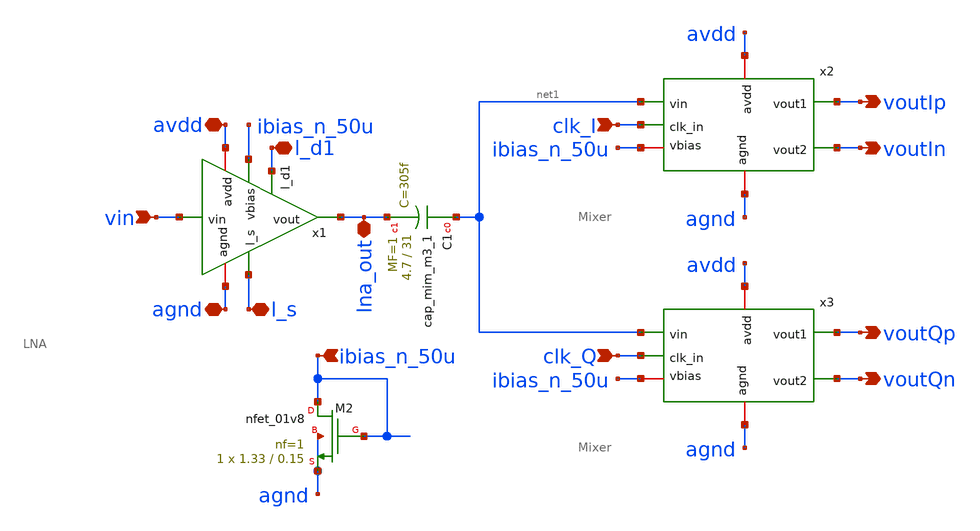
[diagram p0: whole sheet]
** sch_path: Testbenches/LNA_Mixer.sch
**.subckt LNA_Mixer lna_out avdd l_s clk_I clk_Q voutIp voutIn voutQp voutQn vin l_d1 agnd
*+ ibias_n_50u
*.iopin lna_out
*.iopin avdd
*.iopin l_s
*.ipin clk_I
*.ipin clk_Q
*.opin voutIp
*.opin voutIn
*.opin voutQp
*.opin voutQn
*.ipin vin
*.iopin l_d1
*.iopin agnd
*.ipin ibias_n_50u
XC1 net1 lna_out sky130_fd_pr__cap_mim_m3_1 W=4.7 L=31 MF=1 m=1
XM2 ibias_n_50u ibias_n_50u agnd agnd sky130_fd_pr__nfet_01v8 L=0.15 W=1.33 nf=1 ad='int((nf+1)/2) * W/nf * 0.29'
+ as='int((nf+2)/2) * W/nf * 0.29' pd='2*int((nf+1)/2) * (W/nf + 0.29)' ps='2*int((nf+2)/2) * (W/nf + 0.29)'
+ nrd='0.29 / W' nrs='0.29 / W' sa=0 sb=0 sd=0 mult=1 m=1
x1 avdd lna_out vin agnd ibias_n_50u l_s l_d1 LNA
x2 avdd clk_I voutIp voutIn agnd net1 ibias_n_50u Mixer
x3 avdd clk_Q voutQp voutQn agnd net1 ibias_n_50u Mixer
**.ends

* expanding   symbol:  /foss/designs/EE437/Project/ee437-quantum-controller/LNA/LNA.sym # of pins=7
** sym_path: LNA/LNA.sym
** sch_path: LNA/LNA.sch
.subckt LNA avdd vout vin agnd vbias l_s l_d1
*.iopin avdd
*.iopin agnd
*.opin vout
*.ipin vbias
*.iopin vin
*.iopin l_s
*.iopin l_d1
XM1 net1 vin l_s agnd sky130_fd_pr__nfet_01v8 L=0.15 W=8.7 nf=10 ad='int((nf+1)/2) * W/nf * 0.29' as='int((nf+2)/2) * W/nf * 0.29'
+ pd='2*int((nf+1)/2) * (W/nf + 0.29)' ps='2*int((nf+2)/2) * (W/nf + 0.29)' nrd='0.29 / W' nrs='0.29 / W'
+ sa=0 sb=0 sd=0 mult=1 m=1
XC1 avdd l_d1 sky130_fd_pr__cap_mim_m3_1 W=10.5 L=10.5 MF=1 m=1
XM2 l_d1 avdd net1 agnd sky130_fd_pr__nfet_01v8 L=0.15 W=8.7 nf=10 ad='int((nf+1)/2) * W/nf * 0.29' as='int((nf+2)/2) * W/nf * 0.29'
+ pd='2*int((nf+1)/2) * (W/nf + 0.29)' ps='2*int((nf+2)/2) * (W/nf + 0.29)' nrd='0.29 / W' nrs='0.29 / W'
+ sa=0 sb=0 sd=0 mult=1 m=1
XM3 net2 net3 agnd agnd sky130_fd_pr__nfet_01v8 L=0.15 W=8.7 nf=10 ad='int((nf+1)/2) * W/nf * 0.29' as='int((nf+2)/2) * W/nf * 0.29'
+ pd='2*int((nf+1)/2) * (W/nf + 0.29)' ps='2*int((nf+2)/2) * (W/nf + 0.29)' nrd='0.29 / W' nrs='0.29 / W'
+ sa=0 sb=0 sd=0 mult=1 m=1
XM4 vout avdd net2 agnd sky130_fd_pr__nfet_01v8 L=0.15 W=8.7 nf=10 ad='int((nf+1)/2) * W/nf * 0.29' as='int((nf+2)/2) * W/nf * 0.29'
+ pd='2*int((nf+1)/2) * (W/nf + 0.29)' ps='2*int((nf+2)/2) * (W/nf + 0.29)' nrd='0.29 / W' nrs='0.29 / W'
+ sa=0 sb=0 sd=0 mult=1 m=1
XC4 avdd vout sky130_fd_pr__cap_mim_m3_1 W=10.5 L=10.5 MF=1 m=1
XC5 net3 l_d1 sky130_fd_pr__cap_mim_m3_1 W=3.5 L=5.1 MF=1 m=1
XR3 vin net4 agnd sky130_fd_pr__res_xhigh_po_0p35 L=3.5 mult=1 m=1
XR4 net4 net5 agnd sky130_fd_pr__res_xhigh_po_0p35 L=3.5 mult=1 m=1
XR5 net5 net6 agnd sky130_fd_pr__res_xhigh_po_0p35 L=3.5 mult=1 m=1
XR6 net6 net7 agnd sky130_fd_pr__res_xhigh_po_0p35 L=3.5 mult=1 m=1
XR7 net7 vbias agnd sky130_fd_pr__res_xhigh_po_0p35 L=3.5 mult=1 m=1
XR1 net3 net8 agnd sky130_fd_pr__res_xhigh_po_0p35 L=3.5 mult=1 m=1
XR2 net8 net9 agnd sky130_fd_pr__res_xhigh_po_0p35 L=3.5 mult=1 m=1
XR8 net9 net10 agnd sky130_fd_pr__res_xhigh_po_0p35 L=3.5 mult=1 m=1
XR9 net10 net11 agnd sky130_fd_pr__res_xhigh_po_0p35 L=3.5 mult=1 m=1
XR10 net11 vbias agnd sky130_fd_pr__res_xhigh_po_0p35 L=3.5 mult=1 m=1
XC2 net3 l_d1 sky130_fd_pr__cap_mim_m3_1 W=25 L=5 MF=1 m=1
.ends


* expanding   symbol:  /foss/designs/EE437/Project/ee437-quantum-controller/Mixer/Mixer.sym # of
*+ pins=7
** sym_path: Mixer/Mixer.sym
** sch_path: Mixer/Mixer.sch
.subckt Mixer avdd clk_in vout1 vout2 agnd vin vbias
*.ipin vin
*.ipin clk_in
*.iopin avdd
*.iopin agnd
*.opin vout2
*.opin vout1
*.ipin vbias
XM1 net1 clk vin vin sky130_fd_pr__nfet_01v8 L=0.15 W=1 nf=1 ad='int((nf+1)/2) * W/nf * 0.29' as='int((nf+2)/2) * W/nf * 0.29'
+ pd='2*int((nf+1)/2) * (W/nf + 0.29)' ps='2*int((nf+2)/2) * (W/nf + 0.29)' nrd='0.29 / W' nrs='0.29 / W'
+ sa=0 sb=0 sd=0 mult=1 m=1
XM2 net2 clk_bar vin vin sky130_fd_pr__nfet_01v8 L=0.15 W=1 nf=1 ad='int((nf+1)/2) * W/nf * 0.29' as='int((nf+2)/2) * W/nf * 0.29'
+ pd='2*int((nf+1)/2) * (W/nf + 0.29)' ps='2*int((nf+2)/2) * (W/nf + 0.29)' nrd='0.29 / W' nrs='0.29 / W'
+ sa=0 sb=0 sd=0 mult=1 m=1
XM3 vout1 net2 agnd agnd sky130_fd_pr__nfet_01v8 L=1 W=6 nf=12 ad='int((nf+1)/2) * W/nf * 0.29' as='int((nf+2)/2) * W/nf * 0.29'
+ pd='2*int((nf+1)/2) * (W/nf + 0.29)' ps='2*int((nf+2)/2) * (W/nf + 0.29)' nrd='0.29 / W' nrs='0.29 / W'
+ sa=0 sb=0 sd=0 mult=4 m=4
XM4 vout2 net1 agnd agnd sky130_fd_pr__nfet_01v8 L=1 W=6 nf=12 ad='int((nf+1)/2) * W/nf * 0.29' as='int((nf+2)/2) * W/nf * 0.29'
+ pd='2*int((nf+1)/2) * (W/nf + 0.29)' ps='2*int((nf+2)/2) * (W/nf + 0.29)' nrd='0.29 / W' nrs='0.29 / W'
+ sa=0 sb=0 sd=0 mult=4 m=4
XR1 vout2 avdd agnd sky130_fd_pr__res_xhigh_po_0p35 L=0.7 mult=1 m=1
XR2 vout1 avdd agnd sky130_fd_pr__res_xhigh_po_0p35 L=0.7 mult=1 m=1
XR3 net3 vbias agnd sky130_fd_pr__res_xhigh_po_0p35 L=1 mult=1 m=1
XM6 clk_bar clk_in avdd avdd sky130_fd_pr__pfet_01v8 L=0.15 W=2 nf=1 ad='int((nf+1)/2) * W/nf * 0.29'
+ as='int((nf+2)/2) * W/nf * 0.29' pd='2*int((nf+1)/2) * (W/nf + 0.29)' ps='2*int((nf+2)/2) * (W/nf + 0.29)'
+ nrd='0.29 / W' nrs='0.29 / W' sa=0 sb=0 sd=0 mult=1 m=1
XM5 clk_bar clk_in agnd agnd sky130_fd_pr__nfet_01v8 L=0.15 W=1 nf=1 ad='int((nf+1)/2) * W/nf * 0.29'
+ as='int((nf+2)/2) * W/nf * 0.29' pd='2*int((nf+1)/2) * (W/nf + 0.29)' ps='2*int((nf+2)/2) * (W/nf + 0.29)'
+ nrd='0.29 / W' nrs='0.29 / W' sa=0 sb=0 sd=0 mult=1 m=1
XM7 clk clk_bar avdd avdd sky130_fd_pr__pfet_01v8 L=0.15 W=2 nf=1 ad='int((nf+1)/2) * W/nf * 0.29' as='int((nf+2)/2) * W/nf * 0.29'
+ pd='2*int((nf+1)/2) * (W/nf + 0.29)' ps='2*int((nf+2)/2) * (W/nf + 0.29)' nrd='0.29 / W' nrs='0.29 / W'
+ sa=0 sb=0 sd=0 mult=1 m=1
XM8 clk clk_bar agnd agnd sky130_fd_pr__nfet_01v8 L=0.15 W=1 nf=1 ad='int((nf+1)/2) * W/nf * 0.29' as='int((nf+2)/2) * W/nf * 0.29'
+ pd='2*int((nf+1)/2) * (W/nf + 0.29)' ps='2*int((nf+2)/2) * (W/nf + 0.29)' nrd='0.29 / W' nrs='0.29 / W'
+ sa=0 sb=0 sd=0 mult=1 m=1
XR4 vin net3 agnd sky130_fd_pr__res_xhigh_po_0p35 L=1 mult=1 m=1
.ends

.end
